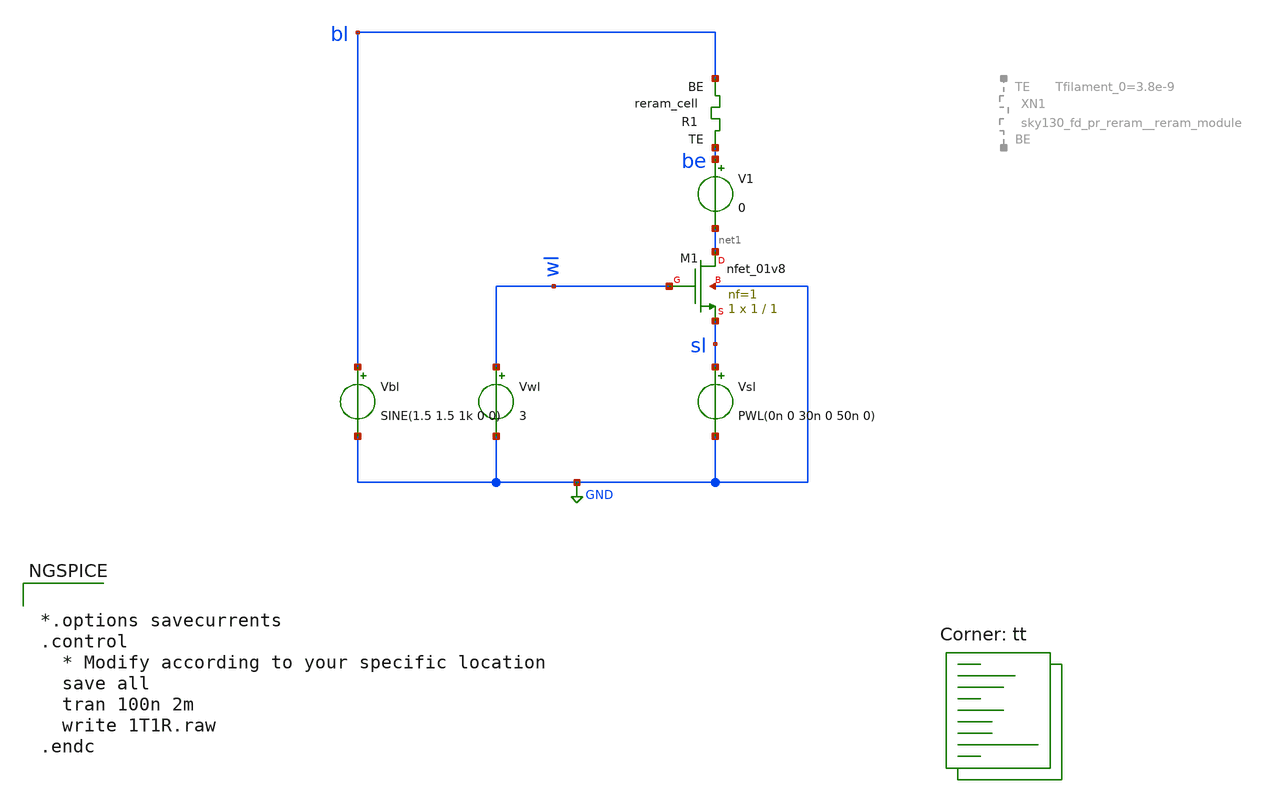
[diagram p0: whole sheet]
** sch_path: Synapse/1T1R.sch
**.subckt 1T1R
XM1 net1 wl sl GND sky130_fd_pr__nfet_01v8 L=1 W=1 nf=1 ad='int((nf+1)/2) * W/nf * 0.29' as='int((nf+2)/2) * W/nf * 0.29'
+ pd='2*int((nf+1)/2) * (W/nf + 0.29)' ps='2*int((nf+2)/2) * (W/nf + 0.29)' nrd='0.29 / W' nrs='0.29 / W'
+ sa=0 sb=0 sd=0 mult=1 m=1
Vbl bl GND SINE(1.5 1.5 1k 0 0)
Vwl wl GND 3
Vsl sl GND PWL(0n 0 30n 0 50n 0)
V1 be net1 0
XR1 be bl sky130_fd_pr_reram__reram_cell Tfilament_0=3.38e-9
**** begin user architecture code


*.options savecurrents
.control
  * Modify according to your specific location
  save all
  tran 100n 2m
  write 1T1R.raw
.endc



.lib $::SKYWATER_MODELS/sky130.lib.spice tt

** opencircuitdesign pdks install
.inc $::SKYWATER_MODELS/sky130_fd_pr_reram__reram_cell.spice

**** end user architecture code
**.ends
.GLOBAL GND
.end
